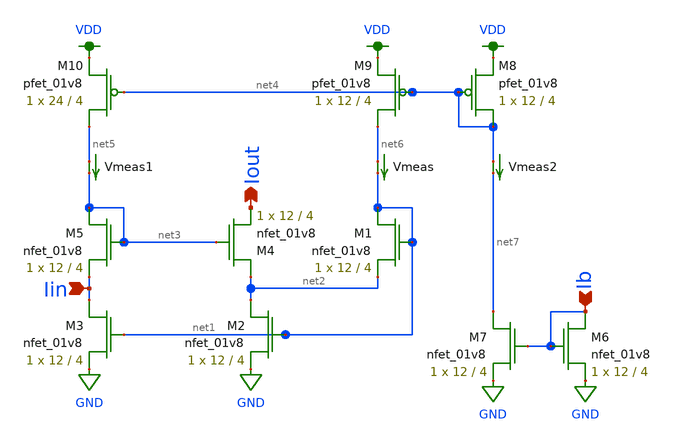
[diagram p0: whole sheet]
** sch_path: modules/super_wilson.sch
**.subckt super_wilson Iin Iout Ib
*.ipin Iin
*.opin Iout
*.ipin Ib
XM6 Ib Ib GND GND sky130_fd_pr__nfet_01v8 L=4 W=12 nf=1 ad='int((nf+1)/2) * W/nf * 0.29' as='int((nf+2)/2) * W/nf * 0.29'
+ pd='2*int((nf+1)/2) * (W/nf + 0.29)' ps='2*int((nf+2)/2) * (W/nf + 0.29)' nrd='0.29 / W' nrs='0.29 / W'
+ sa=0 sb=0 sd=0 mult=1 m=1
XM9 net6 net4 VDD VDD sky130_fd_pr__pfet_01v8 L=4 W=12 nf=1 ad='int((nf+1)/2) * W/nf * 0.29' as='int((nf+2)/2) * W/nf * 0.29'
+ pd='2*int((nf+1)/2) * (W/nf + 0.29)' ps='2*int((nf+2)/2) * (W/nf + 0.29)' nrd='0.29 / W' nrs='0.29 / W'
+ sa=0 sb=0 sd=0 mult=1 m=1
XM10 net5 net4 VDD VDD sky130_fd_pr__pfet_01v8 L=4 W=24 nf=1 ad='int((nf+1)/2) * W/nf * 0.29' as='int((nf+2)/2) * W/nf * 0.29'
+ pd='2*int((nf+1)/2) * (W/nf + 0.29)' ps='2*int((nf+2)/2) * (W/nf + 0.29)' nrd='0.29 / W' nrs='0.29 / W'
+ sa=0 sb=0 sd=0 mult=1 m=1
XM8 net4 net4 VDD VDD sky130_fd_pr__pfet_01v8 L=4 W=12 nf=1 ad='int((nf+1)/2) * W/nf * 0.29' as='int((nf+2)/2) * W/nf * 0.29'
+ pd='2*int((nf+1)/2) * (W/nf + 0.29)' ps='2*int((nf+2)/2) * (W/nf + 0.29)' nrd='0.29 / W' nrs='0.29 / W'
+ sa=0 sb=0 sd=0 mult=1 m=1
XM7 net7 Ib GND GND sky130_fd_pr__nfet_01v8 L=4 W=12 nf=1 ad='int((nf+1)/2) * W/nf * 0.29' as='int((nf+2)/2) * W/nf * 0.29'
+ pd='2*int((nf+1)/2) * (W/nf + 0.29)' ps='2*int((nf+2)/2) * (W/nf + 0.29)' nrd='0.29 / W' nrs='0.29 / W'
+ sa=0 sb=0 sd=0 mult=1 m=1
XM1 net1 net1 net2 GND sky130_fd_pr__nfet_01v8 L=4 W=12 nf=1 ad='int((nf+1)/2) * W/nf * 0.29' as='int((nf+2)/2) * W/nf * 0.29'
+ pd='2*int((nf+1)/2) * (W/nf + 0.29)' ps='2*int((nf+2)/2) * (W/nf + 0.29)' nrd='0.29 / W' nrs='0.29 / W'
+ sa=0 sb=0 sd=0 mult=1 m=1
XM2 net2 net1 GND GND sky130_fd_pr__nfet_01v8 L=4 W=12 nf=1 ad='int((nf+1)/2) * W/nf * 0.29' as='int((nf+2)/2) * W/nf * 0.29'
+ pd='2*int((nf+1)/2) * (W/nf + 0.29)' ps='2*int((nf+2)/2) * (W/nf + 0.29)' nrd='0.29 / W' nrs='0.29 / W'
+ sa=0 sb=0 sd=0 mult=1 m=1
XM3 Iin net1 GND GND sky130_fd_pr__nfet_01v8 L=4 W=12 nf=1 ad='int((nf+1)/2) * W/nf * 0.29' as='int((nf+2)/2) * W/nf * 0.29'
+ pd='2*int((nf+1)/2) * (W/nf + 0.29)' ps='2*int((nf+2)/2) * (W/nf + 0.29)' nrd='0.29 / W' nrs='0.29 / W'
+ sa=0 sb=0 sd=0 mult=1 m=1
XM5 net3 net3 Iin GND sky130_fd_pr__nfet_01v8 L=4 W=12 nf=1 ad='int((nf+1)/2) * W/nf * 0.29' as='int((nf+2)/2) * W/nf * 0.29'
+ pd='2*int((nf+1)/2) * (W/nf + 0.29)' ps='2*int((nf+2)/2) * (W/nf + 0.29)' nrd='0.29 / W' nrs='0.29 / W'
+ sa=0 sb=0 sd=0 mult=1 m=1
XM4 net2 net3 Iout GND sky130_fd_pr__nfet_01v8 L=4 W=12 nf=1 ad='int((nf+1)/2) * W/nf * 0.29' as='int((nf+2)/2) * W/nf * 0.29'
+ pd='2*int((nf+1)/2) * (W/nf + 0.29)' ps='2*int((nf+2)/2) * (W/nf + 0.29)' nrd='0.29 / W' nrs='0.29 / W'
+ sa=0 sb=0 sd=0 mult=1 m=1
Vmeas net6 net1 0
.save i(vmeas)
Vmeas1 net5 net3 0
.save i(vmeas1)
Vmeas2 net4 net7 0
.save i(vmeas2)
**.ends
.GLOBAL GND
.GLOBAL VDD
.end
